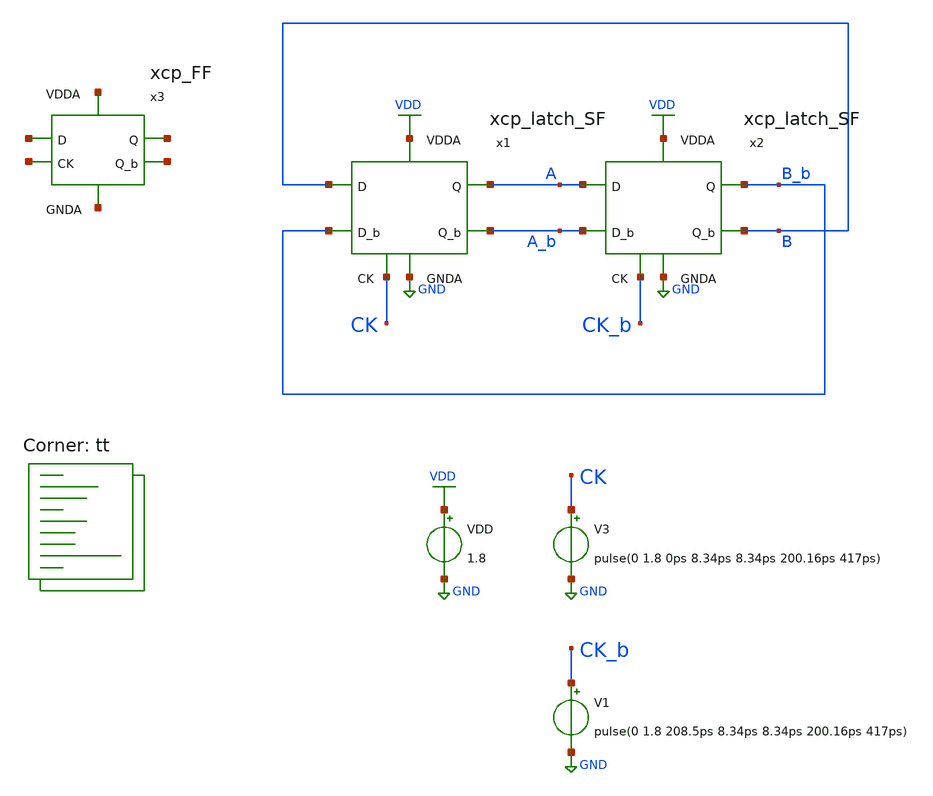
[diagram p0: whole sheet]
** sch_path: projects/pll/divider/xschem_ngspice/tb_xcp_latch_SF.sch
**.subckt tb_xcp_latch_SF
VDD VDD GND 1.8
V3 CK GND pulse(0 1.8 0ps 8.34ps 8.34ps 200.16ps 417ps)
V1 CK_b GND pulse(0 1.8 208.5ps 8.34ps 8.34ps 200.16ps 417ps)
x2 VDD B B_b A_b A CK_b GND xcp_latch_SF
x1 VDD A_b A B_b B CK GND xcp_latch_SF
x3 net1 net2 net3 net4 net5 net6 xcp_FF
**** begin user architecture code



.include /foss/pdks/sky130A/libs.ref/sky130_fd_sc_hd/spice/sky130_fd_sc_hd.spice

.option method=gear
.option wnflag=1
* .option savecurrents

.save @m.x1.xm1.msky130_fd_pr__nfet_01v8[gm] @m.x1.xm2.msky130_fd_pr__nfet_01v8[gm] @m.x1.xm3.msky130_fd_pr__pfet_01v8[gm] @m.x1.xm4.msky130_fd_pr__pfet_01v8[gm] @m.x1.xm5.msky130_fd_pr__nfet_01v8[gm] @m.x1.xm6.msky130_fd_pr__nfet_01v8[gm] @m.x1.xm7.msky130_fd_pr__nfet_01v8[gm] @m.x5.xm1.msky130_fd_pr__nfet_01v8[gm] @m.x5.xm2.msky130_fd_pr__nfet_01v8[gm] @m.x5.xm3.msky130_fd_pr__pfet_01v8[gm] @m.x5.xm4.msky130_fd_pr__pfet_01v8[gm] @m.x5.xm5.msky130_fd_pr__nfet_01v8[gm] @m.x5.xm6.msky130_fd_pr__nfet_01v8[gm] @m.x5.xm7.msky130_fd_pr__nfet_01v8[gm] @v.x1.vmeas @v.x1.vmeas1 @v.x1.vmeas2 @v.x5.vmeas @v.x5.vmeas1 @v.x5.vmeas2


*.ic v(q_b)=1.8

.control

  save v(a) v(a_b) v(b) v(b_b) v(ck)
  * save all
  *tran 0.1n 1u
  tran 0.2p 5n
  *ac dec 20 1 1T
  remzerovec
  write tb_xcp_latch_SF.raw
  set appendwrite

.endc



.lib $::SKYWATER_MODELS/sky130.lib.spice tt
**** end user architecture code
**.ends

* expanding   symbol:  /foss/designs/my_design/projects/pll/divider/xschem_ngspice/xcp_latch_SF.sym
*+ # of pins=7
** sym_path: projects/pll/divider/xschem_ngspice/xcp_latch_SF.sym
** sch_path: projects/pll/divider/xschem_ngspice/xcp_latch_SF.sch
.subckt xcp_latch_SF VDDA Q_b Q D_b D CK GNDA
*.ipin D
*.opin Q
*.ipin D_b
*.ipin CK
*.opin Q_b
*.ipin VDDA
*.ipin GNDA
XM5 net1 CK GNDA GNDA sky130_fd_pr__nfet_01v8 L=0.15 W=2 nf=2 ad='int((nf+1)/2) * W/nf * 0.29' as='int((nf+2)/2) * W/nf * 0.29'
+ pd='2*int((nf+1)/2) * (W/nf + 0.29)' ps='2*int((nf+2)/2) * (W/nf + 0.29)' nrd='0.29 / W' nrs='0.29 / W'
+ sa=0 sb=0 sd=0 mult=1 m=1
XM1 net3 D V_common GNDA sky130_fd_pr__nfet_01v8 L=0.15 W=1 nf=1 ad='int((nf+1)/2) * W/nf * 0.29' as='int((nf+2)/2) * W/nf * 0.29'
+ pd='2*int((nf+1)/2) * (W/nf + 0.29)' ps='2*int((nf+2)/2) * (W/nf + 0.29)' nrd='0.29 / W' nrs='0.29 / W'
+ sa=0 sb=0 sd=0 mult=1 m=1
XM2 net2 D_b V_common GNDA sky130_fd_pr__nfet_01v8 L=0.15 W=1 nf=1 ad='int((nf+1)/2) * W/nf * 0.29' as='int((nf+2)/2) * W/nf * 0.29'
+ pd='2*int((nf+1)/2) * (W/nf + 0.29)' ps='2*int((nf+2)/2) * (W/nf + 0.29)' nrd='0.29 / W' nrs='0.29 / W'
+ sa=0 sb=0 sd=0 mult=1 m=1
Vmeas V_common net1 0
.save i(vmeas)
Vmeas1 Q_b net3 0
.save i(vmeas1)
Vmeas2 Q net2 0
.save i(vmeas2)
XM3 Q_b Q VDDA VDDA sky130_fd_pr__pfet_01v8 L=0.15 W=1 nf=1 ad='int((nf+1)/2) * W/nf * 0.29' as='int((nf+2)/2) * W/nf * 0.29'
+ pd='2*int((nf+1)/2) * (W/nf + 0.29)' ps='2*int((nf+2)/2) * (W/nf + 0.29)' nrd='0.29 / W' nrs='0.29 / W'
+ sa=0 sb=0 sd=0 mult=1 m=1
XM4 Q Q_b VDDA VDDA sky130_fd_pr__pfet_01v8 L=0.15 W=1 nf=1 ad='int((nf+1)/2) * W/nf * 0.29' as='int((nf+2)/2) * W/nf * 0.29'
+ pd='2*int((nf+1)/2) * (W/nf + 0.29)' ps='2*int((nf+2)/2) * (W/nf + 0.29)' nrd='0.29 / W' nrs='0.29 / W'
+ sa=0 sb=0 sd=0 mult=1 m=1
XM6 VDDA D net2 GNDA sky130_fd_pr__nfet_01v8 L=0.15 W=1 nf=1 ad='int((nf+1)/2) * W/nf * 0.29' as='int((nf+2)/2) * W/nf * 0.29'
+ pd='2*int((nf+1)/2) * (W/nf + 0.29)' ps='2*int((nf+2)/2) * (W/nf + 0.29)' nrd='0.29 / W' nrs='0.29 / W'
+ sa=0 sb=0 sd=0 mult=1 m=1
XM7 VDDA D_b net3 GNDA sky130_fd_pr__nfet_01v8 L=0.15 W=1 nf=1 ad='int((nf+1)/2) * W/nf * 0.29' as='int((nf+2)/2) * W/nf * 0.29'
+ pd='2*int((nf+1)/2) * (W/nf + 0.29)' ps='2*int((nf+2)/2) * (W/nf + 0.29)' nrd='0.29 / W' nrs='0.29 / W'
+ sa=0 sb=0 sd=0 mult=1 m=1
.ends


* expanding   symbol:  /foss/designs/my_design/projects/pll/divider/xschem_ngspice/xcp_FF.sym # of
*+ pins=6
** sym_path: projects/pll/divider/xschem_ngspice/xcp_FF.sym
** sch_path: projects/pll/divider/xschem_ngspice/xcp_FF.sch
.subckt xcp_FF VDDA D Q Q_b CK GNDA
*.ipin VDDA
*.opin Q
*.ipin CK
*.ipin GNDA
*.ipin D
*.opin Q_b
x1 VDDA A_b A net2 net3 CK GNDA xcp_latch
x2 VDDA Q_b Q A_b A net1 GNDA xcp_latch
XM1 net1 CK GNDA GNDA sky130_fd_pr__nfet_01v8 L=0.15 W=1 nf=1 ad='int((nf+1)/2) * W/nf * 0.29' as='int((nf+2)/2) * W/nf * 0.29'
+ pd='2*int((nf+1)/2) * (W/nf + 0.29)' ps='2*int((nf+2)/2) * (W/nf + 0.29)' nrd='0.29 / W' nrs='0.29 / W'
+ sa=0 sb=0 sd=0 mult=1 m=1
XM2 net1 CK VDDA VDDA sky130_fd_pr__pfet_01v8 L=0.15 W=1 nf=1 ad='int((nf+1)/2) * W/nf * 0.29' as='int((nf+2)/2) * W/nf * 0.29'
+ pd='2*int((nf+1)/2) * (W/nf + 0.29)' ps='2*int((nf+2)/2) * (W/nf + 0.29)' nrd='0.29 / W' nrs='0.29 / W'
+ sa=0 sb=0 sd=0 mult=1 m=1
XM3 net2 D GNDA GNDA sky130_fd_pr__nfet_01v8 L=0.15 W=1 nf=1 ad='int((nf+1)/2) * W/nf * 0.29' as='int((nf+2)/2) * W/nf * 0.29'
+ pd='2*int((nf+1)/2) * (W/nf + 0.29)' ps='2*int((nf+2)/2) * (W/nf + 0.29)' nrd='0.29 / W' nrs='0.29 / W'
+ sa=0 sb=0 sd=0 mult=1 m=1
XM4 net2 D GNDA GNDA sky130_fd_pr__pfet_01v8 L=0.15 W=1 nf=1 ad='int((nf+1)/2) * W/nf * 0.29' as='int((nf+2)/2) * W/nf * 0.29'
+ pd='2*int((nf+1)/2) * (W/nf + 0.29)' ps='2*int((nf+2)/2) * (W/nf + 0.29)' nrd='0.29 / W' nrs='0.29 / W'
+ sa=0 sb=0 sd=0 mult=1 m=1
XM5 net3 GNDA D VDDA sky130_fd_pr__pfet_01v8 L=0.15 W=1 nf=1 ad='int((nf+1)/2) * W/nf * 0.29' as='int((nf+2)/2) * W/nf * 0.29'
+ pd='2*int((nf+1)/2) * (W/nf + 0.29)' ps='2*int((nf+2)/2) * (W/nf + 0.29)' nrd='0.29 / W' nrs='0.29 / W'
+ sa=0 sb=0 sd=0 mult=1 m=1
XM6 net3 VDDA D GNDA sky130_fd_pr__nfet_01v8 L=0.15 W=1 nf=1 ad='int((nf+1)/2) * W/nf * 0.29' as='int((nf+2)/2) * W/nf * 0.29'
+ pd='2*int((nf+1)/2) * (W/nf + 0.29)' ps='2*int((nf+2)/2) * (W/nf + 0.29)' nrd='0.29 / W' nrs='0.29 / W'
+ sa=0 sb=0 sd=0 mult=1 m=1
.ends


* expanding   symbol:  /foss/designs/my_design/projects/pll/divider/xschem_ngspice/xcp_latch.sym #
*+ of pins=7
** sym_path: projects/pll/divider/xschem_ngspice/xcp_latch.sym
** sch_path: projects/pll/divider/xschem_ngspice/xcp_latch.sch
.subckt xcp_latch VDDA Q_b Q D_b D CK GNDA
*.ipin D
*.opin Q
*.ipin D_b
*.ipin CK
*.opin Q_b
*.ipin VDDA
*.ipin GNDA
XM5 net1 CK GNDA GNDA sky130_fd_pr__nfet_01v8 L=0.15 W=2 nf=2 ad='int((nf+1)/2) * W/nf * 0.29' as='int((nf+2)/2) * W/nf * 0.29'
+ pd='2*int((nf+1)/2) * (W/nf + 0.29)' ps='2*int((nf+2)/2) * (W/nf + 0.29)' nrd='0.29 / W' nrs='0.29 / W'
+ sa=0 sb=0 sd=0 mult=1 m=1
XM1 net3 D V_common GNDA sky130_fd_pr__nfet_01v8 L=0.15 W=1 nf=1 ad='int((nf+1)/2) * W/nf * 0.29' as='int((nf+2)/2) * W/nf * 0.29'
+ pd='2*int((nf+1)/2) * (W/nf + 0.29)' ps='2*int((nf+2)/2) * (W/nf + 0.29)' nrd='0.29 / W' nrs='0.29 / W'
+ sa=0 sb=0 sd=0 mult=1 m=1
XM2 net2 D_b V_common GNDA sky130_fd_pr__nfet_01v8 L=0.15 W=1 nf=1 ad='int((nf+1)/2) * W/nf * 0.29' as='int((nf+2)/2) * W/nf * 0.29'
+ pd='2*int((nf+1)/2) * (W/nf + 0.29)' ps='2*int((nf+2)/2) * (W/nf + 0.29)' nrd='0.29 / W' nrs='0.29 / W'
+ sa=0 sb=0 sd=0 mult=1 m=1
Vmeas V_common net1 0
.save i(vmeas)
Vmeas1 Q_b net3 0
.save i(vmeas1)
Vmeas2 Q net2 0
.save i(vmeas2)
XM3 Q_b Q VDDA VDDA sky130_fd_pr__pfet_01v8 L=0.15 W=1 nf=1 ad='int((nf+1)/2) * W/nf * 0.29' as='int((nf+2)/2) * W/nf * 0.29'
+ pd='2*int((nf+1)/2) * (W/nf + 0.29)' ps='2*int((nf+2)/2) * (W/nf + 0.29)' nrd='0.29 / W' nrs='0.29 / W'
+ sa=0 sb=0 sd=0 mult=1 m=1
XM4 Q Q_b VDDA VDDA sky130_fd_pr__pfet_01v8 L=0.15 W=1 nf=1 ad='int((nf+1)/2) * W/nf * 0.29' as='int((nf+2)/2) * W/nf * 0.29'
+ pd='2*int((nf+1)/2) * (W/nf + 0.29)' ps='2*int((nf+2)/2) * (W/nf + 0.29)' nrd='0.29 / W' nrs='0.29 / W'
+ sa=0 sb=0 sd=0 mult=1 m=1
.ends

.GLOBAL GND
.GLOBAL VDD
.end
